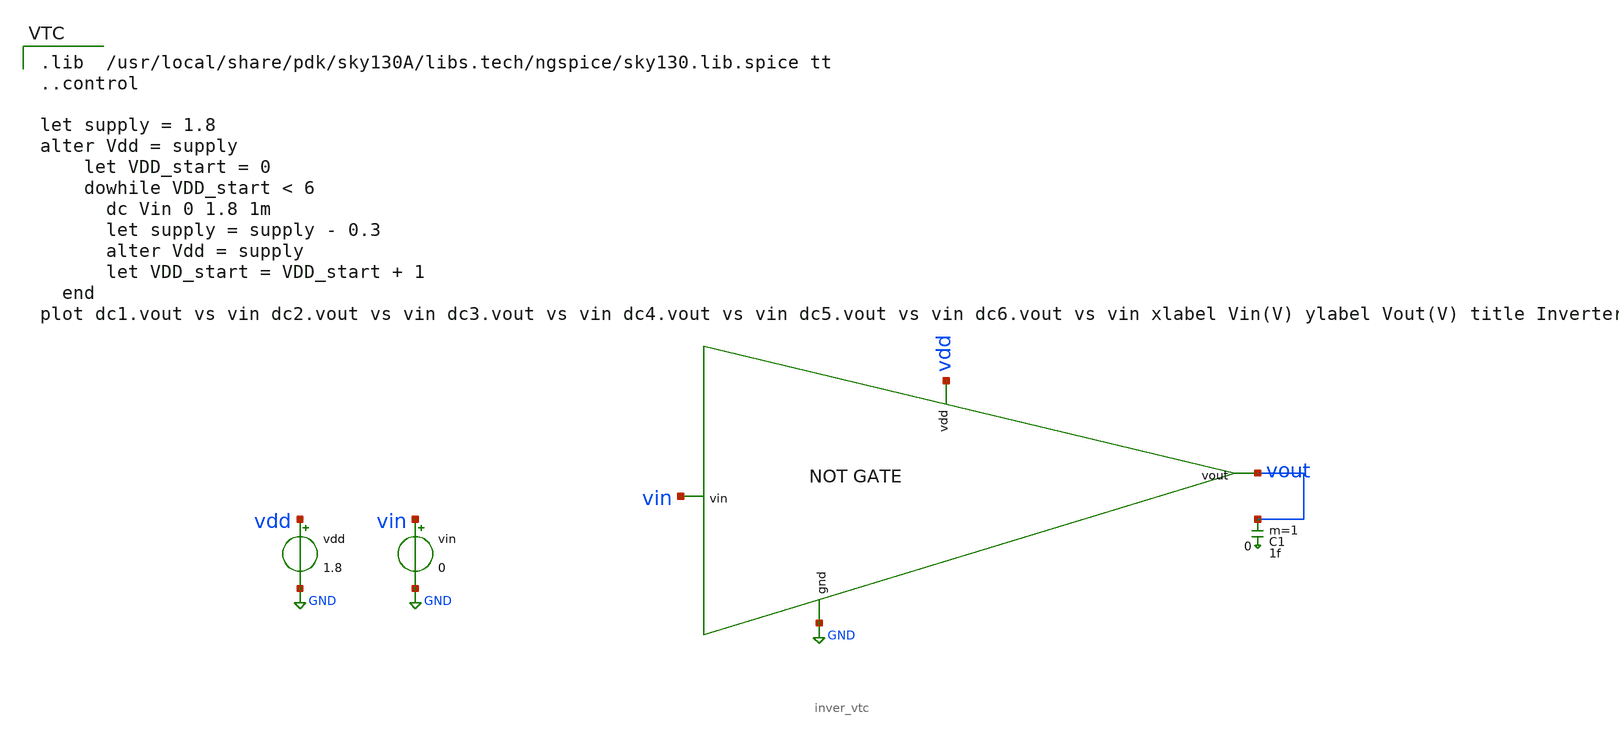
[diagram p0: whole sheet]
** sch_path: Xschem files/POWER_LOAD_inve.sch
**.subckt POWER_LOAD_inve
vin vin GND 0
vdd vdd GND 1.8
x1 vdd vout GND vin inver_vtc
C1 vout 0 1f m=1
**** begin user architecture code

.lib  /usr/local/share/pdk/sky130A/libs.tech/ngspice/sky130.lib.spice tt
..control

let supply = 1.8
alter Vdd = supply
	let VDD_start = 0
	dowhile VDD_start < 6
	  dc Vin 0 1.8 1m
	  let supply = supply - 0.3
	  alter Vdd = supply
	  let VDD_start = VDD_start + 1
  end
plot dc1.vout vs vin dc2.vout vs vin dc3.vout vs vin dc4.vout vs vin dc5.vout vs vin dc6.vout vs vin
+ xlabel Vin(V) ylabel Vout(V) title Inverter

**** end user architecture code
**.ends

* expanding   symbol:  inver_vtc.sym # of pins=4
** sym_path: Xschem files/inver_vtc.sym
** sch_path: Xschem files/inver_vtc.sch
.subckt inver_vtc vdd vout gnd vin
*.ipin vin
*.ipin gnd
*.ipin vdd
*.opin vout
XM1 vout vin vdd vdd sky130_fd_pr__pfet_01v8 L=0.15 W=2 nf=1 ad='int((nf+1)/2) * W/nf * 0.29' as='int((nf+2)/2) * W/nf * 0.29'
+ pd='2*int((nf+1)/2) * (W/nf + 0.29)' ps='2*int((nf+2)/2) * (W/nf + 0.29)' nrd='0.29 / W' nrs='0.29 / W'
+ sa=0 sb=0 sd=0 mult=1 m=1
XM2 vout vin gnd gnd sky130_fd_pr__nfet_01v8 L=0.15 W=1 nf=1 ad='int((nf+1)/2) * W/nf * 0.29' as='int((nf+2)/2) * W/nf * 0.29'
+ pd='2*int((nf+1)/2) * (W/nf + 0.29)' ps='2*int((nf+2)/2) * (W/nf + 0.29)' nrd='0.29 / W' nrs='0.29 / W'
+ sa=0 sb=0 sd=0 mult=1 m=1
.ends

.GLOBAL GND
.end
